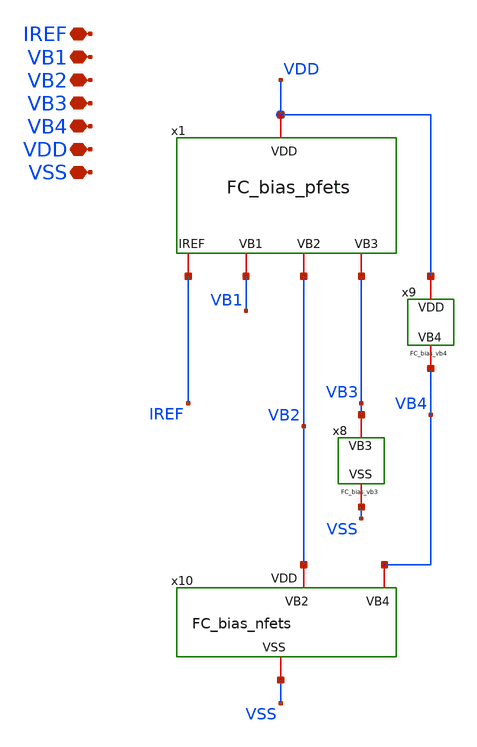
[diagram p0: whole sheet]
** sch_path: Voltage_Reference/LDO/Folded/FC_bias_net.sch
**.subckt FC_bias_net VDD VSS VB2 IREF VB3 VB4 VB1
*.iopin VDD
*.iopin VSS
*.iopin VB2
*.iopin IREF
*.iopin VB3
*.iopin VB4
*.iopin VB1
x8 VB3 VSS FC_bias_vb3
x9 VB4 VDD FC_bias_vb4
x10 VB2 VB4 VSS FC_bias_nfets
x1 VB1 VB2 VB3 IREF VDD FC_bias_pfets
**.ends
.end
